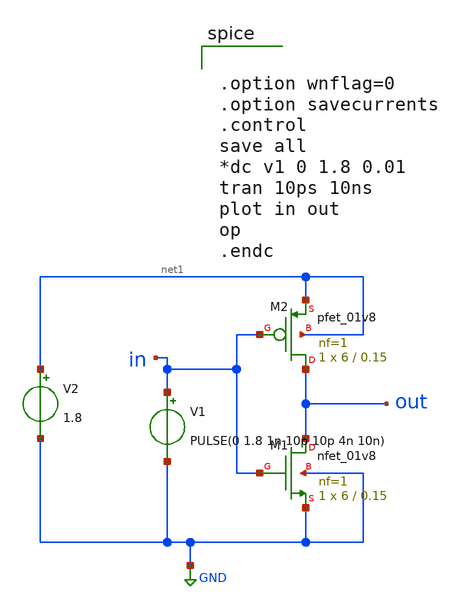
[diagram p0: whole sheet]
** sch_path: inverter.sch
**.subckt inverter
XM1 out in GND GND sky130_fd_pr__nfet_01v8 L=0.15 W=6 nf=1 ad='int((1 + 1)/2) * 6 / 1 * 0.29' as='int((1 + 2)/2) * 6 / 1 * 0.29'
+ pd='2*int((1 + 1)/2) * (6 / 1 + 0.29)' ps='2*int((1 + 2)/2) * (6 / 1 + 0.29)' nrd='0.29 / 6 ' nrs='0.29 / 6 '
+ sa=0 sb=0 sd=0 mult=1 m=1
XM2 out in net1 net1 sky130_fd_pr__pfet_01v8 L=0.15 W=6 nf=1 ad='int((1 + 1)/2) * 6 / 1 * 0.29' as='int((1 + 2)/2) * 6 / 1 * 0.29'
+ pd='2*int((1 + 1)/2) * (6 / 1 + 0.29)' ps='2*int((1 + 2)/2) * (6 / 1 + 0.29)' nrd='0.29 / 6 ' nrs='0.29 / 6 '
+ sa=0 sb=0 sd=0 mult=1 m=1
V1 in GND PULSE(0 1.8 1n 10p 10p 4n 10n)
V2 net1 GND 1.8
**** begin user architecture code
 .lib /foss/pdks/sky130A/libs.tech/ngspice/sky130.lib.spice tt


.option wnflag=0
.option savecurrents
.control
save all
*dc v1 0 1.8 0.01
tran 10ps 10ns
plot in out
op
.endc



**** end user architecture code
**.ends
.GLOBAL GND
.end
